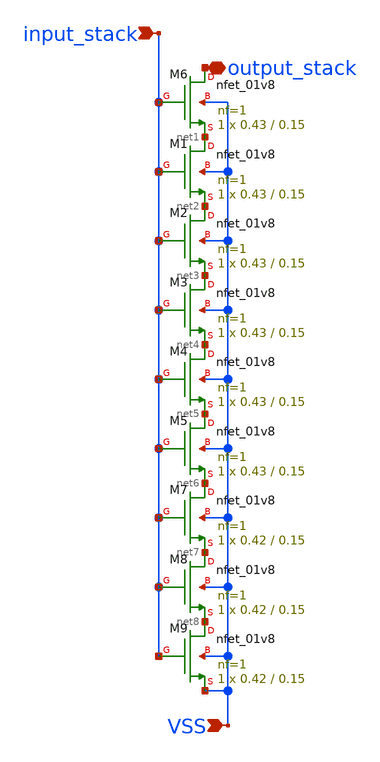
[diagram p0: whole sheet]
** sch_path: hgu/xschem/hgu_nfet_hvt_stack_in_delay.sch
**.subckt hgu_nfet_hvt_stack_in_delay VSS input_stack output_stack
*.ipin VSS
*.ipin input_stack
*.iopin output_stack
XM6 output_stack input_stack net1 VSS sky130_fd_pr__nfet_01v8 L=0.15 W=0.43 nf=1 ad='int((nf+1)/2) * W/nf * 0.29'
+ as='int((nf+2)/2) * W/nf * 0.29' pd='2*int((nf+1)/2) * (W/nf + 0.29)' ps='2*int((nf+2)/2) * (W/nf + 0.29)'
+ nrd='0.29 / W' nrs='0.29 / W' sa=0 sb=0 sd=0 mult=1 m=1
XM1 net1 input_stack net2 VSS sky130_fd_pr__nfet_01v8 L=0.15 W=0.43 nf=1 ad='int((nf+1)/2) * W/nf * 0.29'
+ as='int((nf+2)/2) * W/nf * 0.29' pd='2*int((nf+1)/2) * (W/nf + 0.29)' ps='2*int((nf+2)/2) * (W/nf + 0.29)'
+ nrd='0.29 / W' nrs='0.29 / W' sa=0 sb=0 sd=0 mult=1 m=1
XM2 net2 input_stack net3 VSS sky130_fd_pr__nfet_01v8 L=0.15 W=0.43 nf=1 ad='int((nf+1)/2) * W/nf * 0.29'
+ as='int((nf+2)/2) * W/nf * 0.29' pd='2*int((nf+1)/2) * (W/nf + 0.29)' ps='2*int((nf+2)/2) * (W/nf + 0.29)'
+ nrd='0.29 / W' nrs='0.29 / W' sa=0 sb=0 sd=0 mult=1 m=1
XM3 net3 input_stack net4 VSS sky130_fd_pr__nfet_01v8 L=0.15 W=0.43 nf=1 ad='int((nf+1)/2) * W/nf * 0.29'
+ as='int((nf+2)/2) * W/nf * 0.29' pd='2*int((nf+1)/2) * (W/nf + 0.29)' ps='2*int((nf+2)/2) * (W/nf + 0.29)'
+ nrd='0.29 / W' nrs='0.29 / W' sa=0 sb=0 sd=0 mult=1 m=1
XM4 net4 input_stack net5 VSS sky130_fd_pr__nfet_01v8 L=0.15 W=0.43 nf=1 ad='int((nf+1)/2) * W/nf * 0.29'
+ as='int((nf+2)/2) * W/nf * 0.29' pd='2*int((nf+1)/2) * (W/nf + 0.29)' ps='2*int((nf+2)/2) * (W/nf + 0.29)'
+ nrd='0.29 / W' nrs='0.29 / W' sa=0 sb=0 sd=0 mult=1 m=1
XM5 net5 input_stack net6 VSS sky130_fd_pr__nfet_01v8 L=0.15 W=0.43 nf=1 ad='int((nf+1)/2) * W/nf * 0.29'
+ as='int((nf+2)/2) * W/nf * 0.29' pd='2*int((nf+1)/2) * (W/nf + 0.29)' ps='2*int((nf+2)/2) * (W/nf + 0.29)'
+ nrd='0.29 / W' nrs='0.29 / W' sa=0 sb=0 sd=0 mult=1 m=1
XM7 net6 input_stack net7 VSS sky130_fd_pr__nfet_01v8 L=0.15 W=0.42 nf=1 ad='int((nf+1)/2) * W/nf * 0.29'
+ as='int((nf+2)/2) * W/nf * 0.29' pd='2*int((nf+1)/2) * (W/nf + 0.29)' ps='2*int((nf+2)/2) * (W/nf + 0.29)'
+ nrd='0.29 / W' nrs='0.29 / W' sa=0 sb=0 sd=0 mult=1 m=1
XM8 net7 input_stack net8 VSS sky130_fd_pr__nfet_01v8 L=0.15 W=0.42 nf=1 ad='int((nf+1)/2) * W/nf * 0.29'
+ as='int((nf+2)/2) * W/nf * 0.29' pd='2*int((nf+1)/2) * (W/nf + 0.29)' ps='2*int((nf+2)/2) * (W/nf + 0.29)'
+ nrd='0.29 / W' nrs='0.29 / W' sa=0 sb=0 sd=0 mult=1 m=1
XM9 net8 input_stack VSS VSS sky130_fd_pr__nfet_01v8 L=0.15 W=0.42 nf=1 ad='int((nf+1)/2) * W/nf * 0.29'
+ as='int((nf+2)/2) * W/nf * 0.29' pd='2*int((nf+1)/2) * (W/nf + 0.29)' ps='2*int((nf+2)/2) * (W/nf + 0.29)'
+ nrd='0.29 / W' nrs='0.29 / W' sa=0 sb=0 sd=0 mult=1 m=1
**.ends
.end
